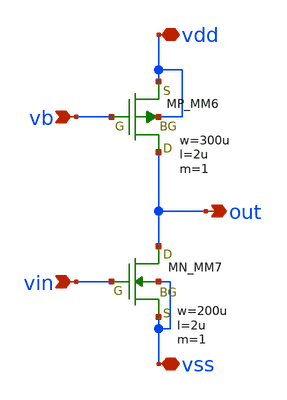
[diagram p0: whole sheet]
** sch_path: member_project/AM_Radio/Yamada3/xschem/cs.sch
**.subckt cs vb vin out vss vdd
*.ipin vb
*.ipin vin
*.opin out
*.iopin vss
*.iopin vdd
MM6 out vb vdd vdd PMOS w=300u l=2u as=0 ad=0 ps=0 pd=0 nrd=0 nrs=0 m=1
MM7 out vin vss vss NMOS w=200u l=2u as=0 ad=0 ps=0 pd=0 nrd=0 nrs=0 m=1
**.ends
.end
